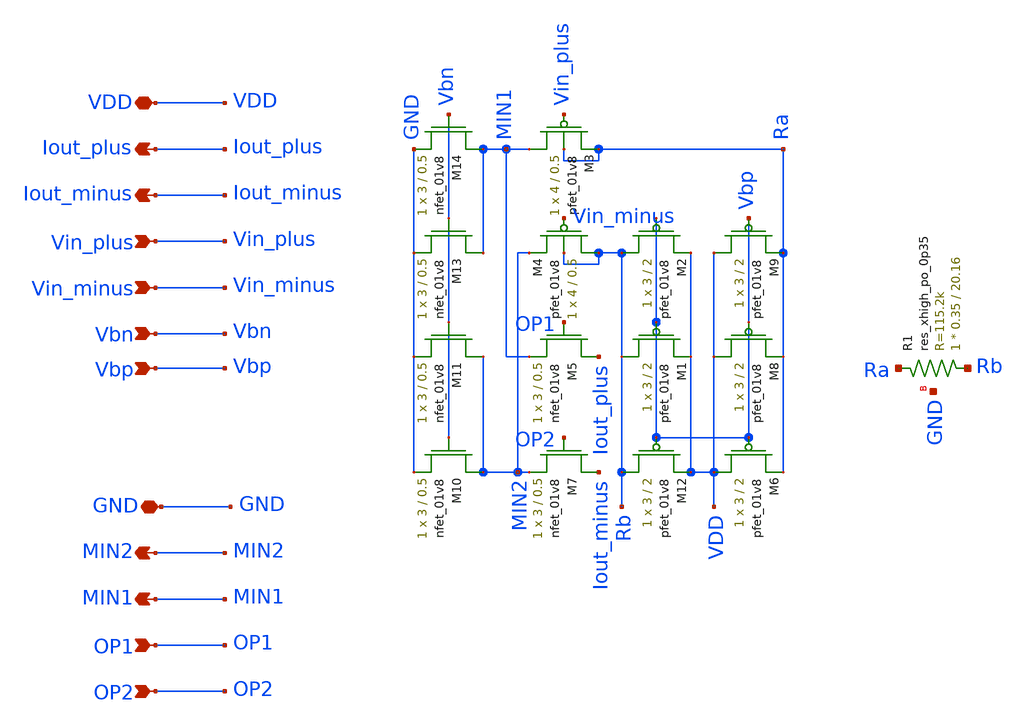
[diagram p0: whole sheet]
** sch_path: final/LDS/brad_VI_input_LDS.sch
**.subckt brad_VI_input_LDS Iout_plus Iout_minus VDD Vin_plus Vin_minus Vbn GND Vbp MIN1 MIN2 OP1
*+ OP2
*.opin Iout_plus
*.opin Iout_minus
*.iopin VDD
*.ipin Vin_plus
*.ipin Vin_minus
*.ipin Vbn
*.iopin GND
*.ipin Vbp
*.opin MIN1
*.opin MIN2
*.ipin OP1
*.ipin OP2
XM3 MIN1 Vin_plus Ra Ra sky130_fd_pr__pfet_01v8 L=0.5 W=4 nf=1 ad='int((nf+1)/2) * W/nf * 0.29' as='int((nf+2)/2) * W/nf * 0.29'
+ pd='2*int((nf+1)/2) * (W/nf + 0.29)' ps='2*int((nf+2)/2) * (W/nf + 0.29)' nrd='0.29 / W' nrs='0.29 / W'
+ sa=0 sb=0 sd=0 mult=1 m=1
XM5 Iout_plus OP1 MIN1 GND sky130_fd_pr__nfet_01v8 L=0.5 W=3 nf=1 ad='int((nf+1)/2) * W/nf * 0.29' as='int((nf+2)/2) * W/nf * 0.29'
+ pd='2*int((nf+1)/2) * (W/nf + 0.29)' ps='2*int((nf+2)/2) * (W/nf + 0.29)' nrd='0.29 / W' nrs='0.29 / W'
+ sa=0 sb=0 sd=0 mult=1 m=1
XM4 Rb Vin_minus MIN2 Rb sky130_fd_pr__pfet_01v8 L=0.5 W=4 nf=1 ad='int((nf+1)/2) * W/nf * 0.29' as='int((nf+2)/2) * W/nf * 0.29'
+ pd='2*int((nf+1)/2) * (W/nf + 0.29)' ps='2*int((nf+2)/2) * (W/nf + 0.29)' nrd='0.29 / W' nrs='0.29 / W'
+ sa=0 sb=0 sd=0 mult=1 m=1
XM6 VDD Vbp Ra VDD sky130_fd_pr__pfet_01v8 L=2 W=3 nf=1 ad='int((nf+1)/2) * W/nf * 0.29' as='int((nf+2)/2) * W/nf * 0.29'
+ pd='2*int((nf+1)/2) * (W/nf + 0.29)' ps='2*int((nf+2)/2) * (W/nf + 0.29)' nrd='0.29 / W' nrs='0.29 / W'
+ sa=0 sb=0 sd=0 mult=1 m=1
XM12 Rb Vbp VDD VDD sky130_fd_pr__pfet_01v8 L=2 W=3 nf=1 ad='int((nf+1)/2) * W/nf * 0.29' as='int((nf+2)/2) * W/nf * 0.29'
+ pd='2*int((nf+1)/2) * (W/nf + 0.29)' ps='2*int((nf+2)/2) * (W/nf + 0.29)' nrd='0.29 / W' nrs='0.29 / W'
+ sa=0 sb=0 sd=0 mult=1 m=1
XR1 Rb Ra GND sky130_fd_pr__res_xhigh_po_0p35 L=20.16 mult=1 m=1
XM1 Rb Vbp VDD VDD sky130_fd_pr__pfet_01v8 L=2 W=3 nf=1 ad='int((nf+1)/2) * W/nf * 0.29' as='int((nf+2)/2) * W/nf * 0.29'
+ pd='2*int((nf+1)/2) * (W/nf + 0.29)' ps='2*int((nf+2)/2) * (W/nf + 0.29)' nrd='0.29 / W' nrs='0.29 / W'
+ sa=0 sb=0 sd=0 mult=1 m=1
XM2 Rb Vbp VDD VDD sky130_fd_pr__pfet_01v8 L=2 W=3 nf=1 ad='int((nf+1)/2) * W/nf * 0.29' as='int((nf+2)/2) * W/nf * 0.29'
+ pd='2*int((nf+1)/2) * (W/nf + 0.29)' ps='2*int((nf+2)/2) * (W/nf + 0.29)' nrd='0.29 / W' nrs='0.29 / W'
+ sa=0 sb=0 sd=0 mult=1 m=1
XM8 VDD Vbp Ra VDD sky130_fd_pr__pfet_01v8 L=2 W=3 nf=1 ad='int((nf+1)/2) * W/nf * 0.29' as='int((nf+2)/2) * W/nf * 0.29'
+ pd='2*int((nf+1)/2) * (W/nf + 0.29)' ps='2*int((nf+2)/2) * (W/nf + 0.29)' nrd='0.29 / W' nrs='0.29 / W'
+ sa=0 sb=0 sd=0 mult=1 m=1
XM9 VDD Vbp Ra VDD sky130_fd_pr__pfet_01v8 L=2 W=3 nf=1 ad='int((nf+1)/2) * W/nf * 0.29' as='int((nf+2)/2) * W/nf * 0.29'
+ pd='2*int((nf+1)/2) * (W/nf + 0.29)' ps='2*int((nf+2)/2) * (W/nf + 0.29)' nrd='0.29 / W' nrs='0.29 / W'
+ sa=0 sb=0 sd=0 mult=1 m=1
XM7 Iout_minus OP2 MIN2 GND sky130_fd_pr__nfet_01v8 L=0.5 W=3 nf=1 ad='int((nf+1)/2) * W/nf * 0.29' as='int((nf+2)/2) * W/nf * 0.29'
+ pd='2*int((nf+1)/2) * (W/nf + 0.29)' ps='2*int((nf+2)/2) * (W/nf + 0.29)' nrd='0.29 / W' nrs='0.29 / W'
+ sa=0 sb=0 sd=0 mult=1 m=1
XM10 MIN2 Vbn GND GND sky130_fd_pr__nfet_01v8 L=0.5 W=3 nf=1 ad='int((nf+1)/2) * W/nf * 0.29' as='int((nf+2)/2) * W/nf * 0.29'
+ pd='2*int((nf+1)/2) * (W/nf + 0.29)' ps='2*int((nf+2)/2) * (W/nf + 0.29)' nrd='0.29 / W' nrs='0.29 / W'
+ sa=0 sb=0 sd=0 mult=1 m=1
XM11 MIN2 Vbn GND GND sky130_fd_pr__nfet_01v8 L=0.5 W=3 nf=1 ad='int((nf+1)/2) * W/nf * 0.29' as='int((nf+2)/2) * W/nf * 0.29'
+ pd='2*int((nf+1)/2) * (W/nf + 0.29)' ps='2*int((nf+2)/2) * (W/nf + 0.29)' nrd='0.29 / W' nrs='0.29 / W'
+ sa=0 sb=0 sd=0 mult=1 m=1
XM13 MIN1 Vbn GND GND sky130_fd_pr__nfet_01v8 L=0.5 W=3 nf=1 ad='int((nf+1)/2) * W/nf * 0.29' as='int((nf+2)/2) * W/nf * 0.29'
+ pd='2*int((nf+1)/2) * (W/nf + 0.29)' ps='2*int((nf+2)/2) * (W/nf + 0.29)' nrd='0.29 / W' nrs='0.29 / W'
+ sa=0 sb=0 sd=0 mult=1 m=1
XM14 MIN1 Vbn GND GND sky130_fd_pr__nfet_01v8 L=0.5 W=3 nf=1 ad='int((nf+1)/2) * W/nf * 0.29' as='int((nf+2)/2) * W/nf * 0.29'
+ pd='2*int((nf+1)/2) * (W/nf + 0.29)' ps='2*int((nf+2)/2) * (W/nf + 0.29)' nrd='0.29 / W' nrs='0.29 / W'
+ sa=0 sb=0 sd=0 mult=1 m=1
**.ends
.end
